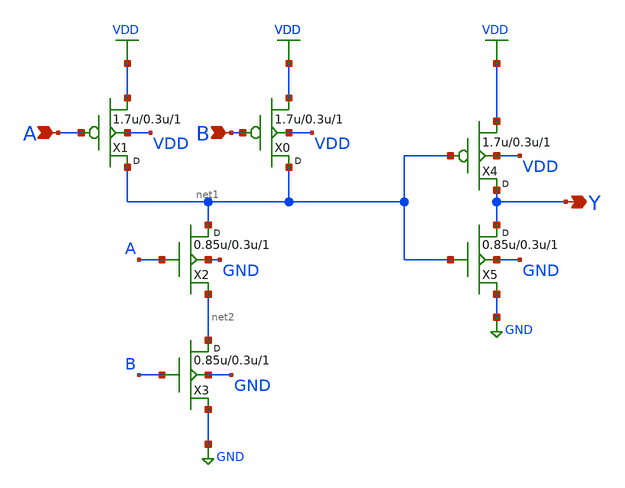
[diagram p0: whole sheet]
** sch_path: gf180mcu_osu_sc_gp9t3v3/cells/and2/gf180mcu_osu_sc_gp9t3v3__and2_1.sch
**.subckt gf180mcu_osu_sc_gp9t3v3__and2_1 A B Y
*.ipin A
*.ipin B
*.opin Y
X1 net1 A VDD VDD pfet_03p3 w=1.7u l=0.3u m=1
X0 net1 B VDD VDD pfet_03p3 w=1.7u l=0.3u m=1
X2 net1 A net2 GND nfet_03p3 w=0.85u l=0.3u m=1
X3 net2 B GND GND nfet_03p3 w=0.85u l=0.3u m=1
X4 Y net1 VDD VDD pfet_03p3 w=1.7u l=0.3u m=1
X5 Y net1 GND GND nfet_03p3 w=0.85u l=0.3u m=1
**.ends
.GLOBAL VDD
.GLOBAL GND
.end
